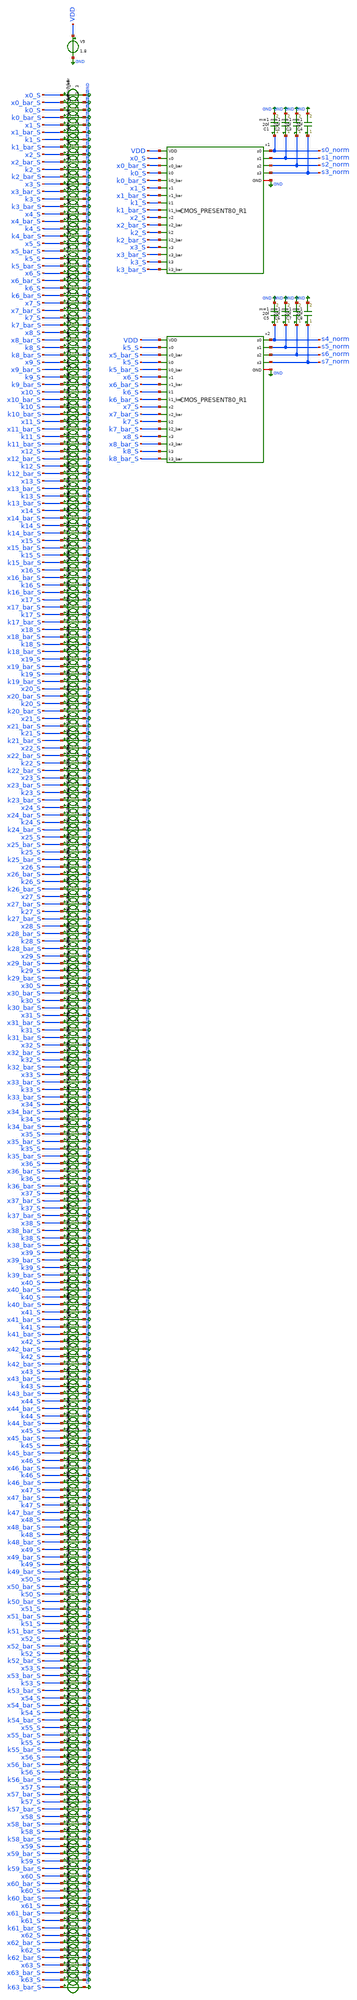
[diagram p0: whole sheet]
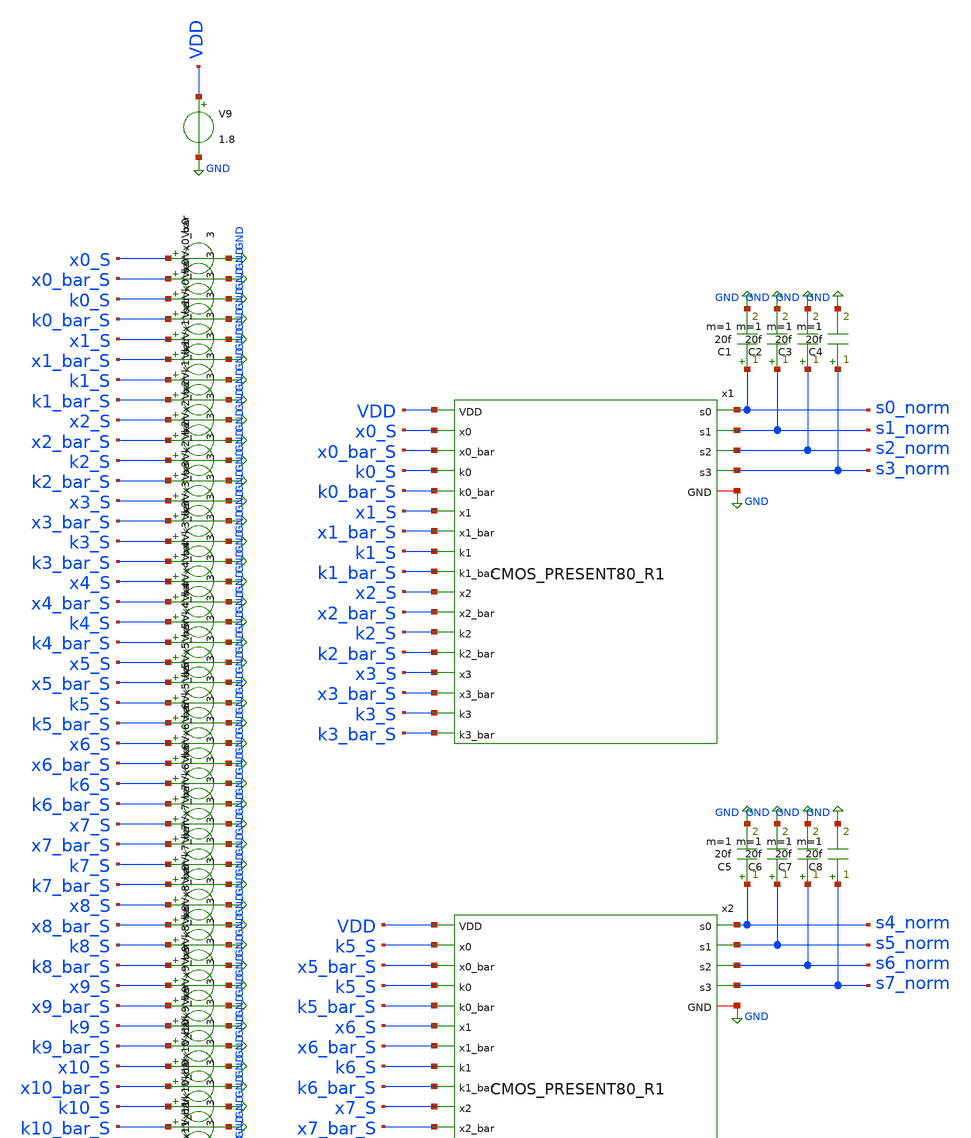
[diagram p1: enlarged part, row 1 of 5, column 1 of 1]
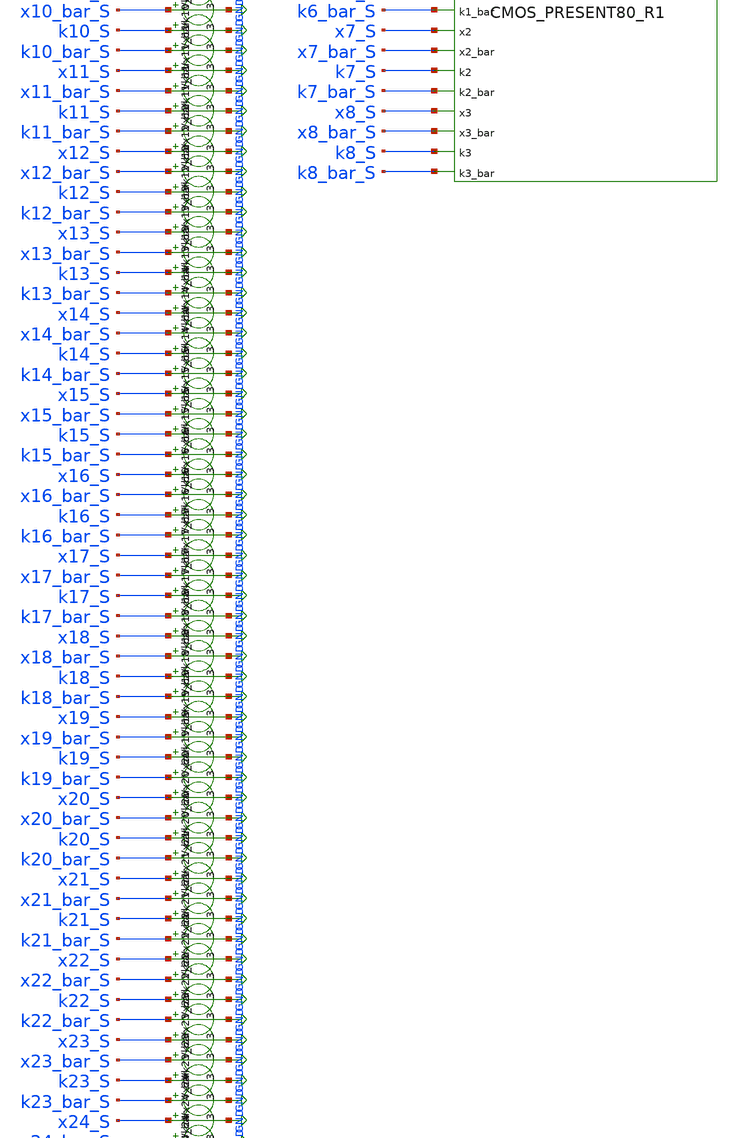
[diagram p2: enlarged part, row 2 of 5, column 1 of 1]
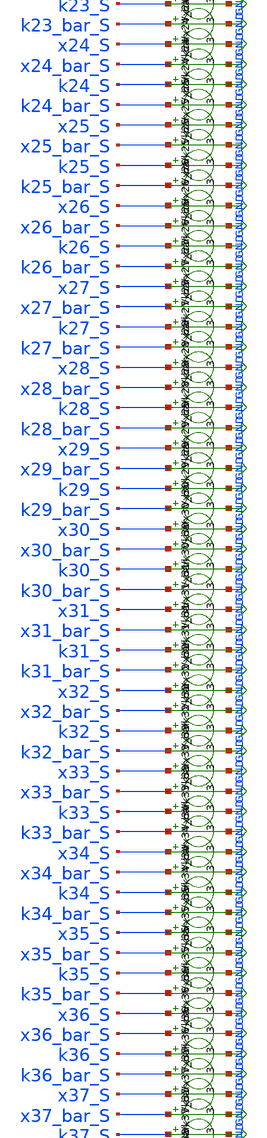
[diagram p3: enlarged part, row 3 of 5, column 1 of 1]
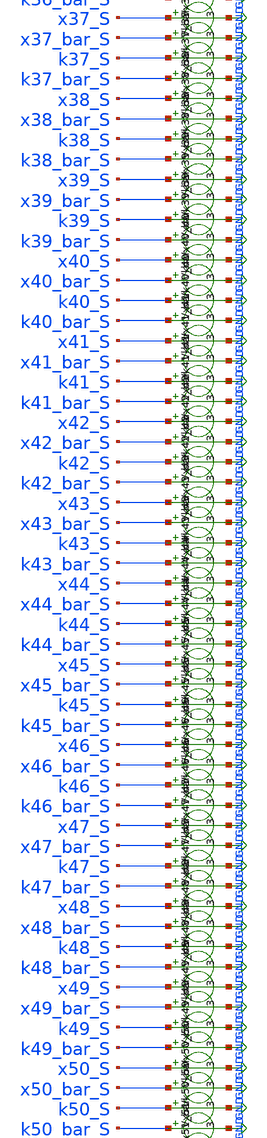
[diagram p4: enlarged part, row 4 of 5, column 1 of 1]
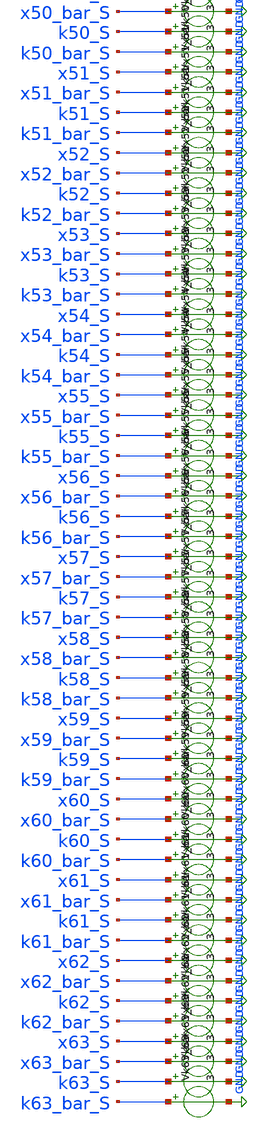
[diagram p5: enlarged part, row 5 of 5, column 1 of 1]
** sch_path: skywater_stuff/CMOS_PRESENT80_R1_sim.sch
**.subckt CMOS_PRESENT80_R1_sim
V9 VDD GND 1.8
C1 s0_norm GND 20f m=1
C2 s1_norm GND 20f m=1
C3 s2_norm GND 20f m=1
C4 s3_norm GND 20f m=1
x1 VDD GND k0_S k0_bar_S x0_S x0_bar_S x1_bar_S x1_S k1_bar_S k1_S k2_S k2_bar_S x2_S x2_bar_S
+ x3_bar_S x3_S k3_bar_S k3_S s3_norm s2_norm s1_norm s0_norm CMOS_PRESENT80_R1
Vx0 x0_S GND 3
Vx0_bar x0_bar_S GND 3
Vk0 k0_S GND 3
Vk0_bar k0_bar_S GND 3
Vx1 x1_S GND 3
Vx1_bar x1_bar_S GND 3
Vk1 k1_S GND 3
Vk1_bar k1_bar_S GND 3
Vx2 x2_S GND 3
Vx2_bar x2_bar_S GND 3
Vk2 k2_S GND 3
Vk2_bar k2_bar_S GND 3
Vx3 x3_S GND 3
Vx3_bar x3_bar_S GND 3
Vk3 k3_S GND 3
Vk3_bar k3_bar_S GND 3
Vx4 x4_S GND 3
Vx4_bar x4_bar_S GND 3
Vk4 k4_S GND 3
Vk4_bar k4_bar_S GND 3
Vx5 x5_S GND 3
Vx5_bar x5_bar_S GND 3
Vk5 k5_S GND 3
Vk5_bar k5_bar_S GND 3
Vx6 x6_S GND 3
Vx6_bar x6_bar_S GND 3
Vk6 k6_S GND 3
Vk6_bar k6_bar_S GND 3
Vx7 x7_S GND 3
Vx7_bar x7_bar_S GND 3
Vk7 k7_S GND 3
Vk7_bar k7_bar_S GND 3
Vx8 x8_S GND 3
Vx8_bar x8_bar_S GND 3
Vk8 k8_S GND 3
Vk8_bar k8_bar_S GND 3
Vx9 x9_S GND 3
Vx9_bar x9_bar_S GND 3
Vk9 k9_S GND 3
Vk9_bar k9_bar_S GND 3
Vx10 x10_S GND 3
Vx10_bar x10_bar_S GND 3
Vk10 k10_S GND 3
Vk10_bar k10_bar_S GND 3
Vx11 x11_S GND 3
Vx11_bar x11_bar_S GND 3
Vk11 k11_S GND 3
Vk11_bar k11_bar_S GND 3
Vx12 x12_S GND 3
Vx12_bar x12_bar_S GND 3
Vk12 k12_S GND 3
Vk12_bar k12_bar_S GND 3
Vx13 x13_S GND 3
Vx13_bar x13_bar_S GND 3
Vk13 k13_S GND 3
Vk13_bar k13_bar_S GND 3
Vx14 x14_S GND 3
Vx14_bar x14_bar_S GND 3
Vk14 k14_S GND 3
Vk14_bar k14_bar_S GND 3
Vx15 x15_S GND 3
Vx15_bar x15_bar_S GND 3
Vk15 k15_S GND 3
Vk15_bar k15_bar_S GND 3
Vx16 x16_S GND 3
Vx16_bar x16_bar_S GND 3
Vk16 k16_S GND 3
Vk16_bar k16_bar_S GND 3
Vx17 x17_S GND 3
Vx17_bar x17_bar_S GND 3
Vk17 k17_S GND 3
Vk17_bar k17_bar_S GND 3
Vx18 x18_S GND 3
Vx18_bar x18_bar_S GND 3
Vk18 k18_S GND 3
Vk18_bar k18_bar_S GND 3
Vx19 x19_S GND 3
Vx19_bar x19_bar_S GND 3
Vk19 k19_S GND 3
Vk19_bar k19_bar_S GND 3
Vx20 x20_S GND 3
Vx20_bar x20_bar_S GND 3
Vk20 k20_S GND 3
Vk20_bar k20_bar_S GND 3
Vx21 x21_S GND 3
Vx21_bar x21_bar_S GND 3
Vk21 k21_S GND 3
Vk21_bar k21_bar_S GND 3
Vx22 x22_S GND 3
Vx22_bar x22_bar_S GND 3
Vk22 k22_S GND 3
Vk22_bar k22_bar_S GND 3
Vx23 x23_S GND 3
Vx23_bar x23_bar_S GND 3
Vk23 k23_S GND 3
Vk23_bar k23_bar_S GND 3
Vx24 x24_S GND 3
Vx24_bar x24_bar_S GND 3
Vk24 k24_S GND 3
Vk24_bar k24_bar_S GND 3
Vx25 x25_S GND 3
Vx25_bar x25_bar_S GND 3
Vk25 k25_S GND 3
Vk25_bar k25_bar_S GND 3
Vx26 x26_S GND 3
Vx26_bar x26_bar_S GND 3
Vk26 k26_S GND 3
Vk26_bar k26_bar_S GND 3
Vx27 x27_S GND 3
Vx27_bar x27_bar_S GND 3
Vk27 k27_S GND 3
Vk27_bar k27_bar_S GND 3
Vx28 x28_S GND 3
Vx28_bar x28_bar_S GND 3
Vk28 k28_S GND 3
Vk28_bar k28_bar_S GND 3
Vx29 x29_S GND 3
Vx29_bar x29_bar_S GND 3
Vk29 k29_S GND 3
Vk29_bar k29_bar_S GND 3
Vx30 x30_S GND 3
Vx30_bar x30_bar_S GND 3
Vk30 k30_S GND 3
Vk30_bar k30_bar_S GND 3
Vx31 x31_S GND 3
Vx31_bar x31_bar_S GND 3
Vk31 k31_S GND 3
Vk31_bar k31_bar_S GND 3
Vx32 x32_S GND 3
Vx32_bar x32_bar_S GND 3
Vk32 k32_S GND 3
Vk32_bar k32_bar_S GND 3
Vx33 x33_S GND 3
Vx33_bar x33_bar_S GND 3
Vk33 k33_S GND 3
Vk33_bar k33_bar_S GND 3
Vx34 x34_S GND 3
Vx34_bar x34_bar_S GND 3
Vk34 k34_S GND 3
Vk34_bar k34_bar_S GND 3
Vx35 x35_S GND 3
Vx35_bar x35_bar_S GND 3
Vk35 k35_S GND 3
Vk35_bar k35_bar_S GND 3
Vx36 x36_S GND 3
Vx36_bar x36_bar_S GND 3
Vk36 k36_S GND 3
Vk36_bar k36_bar_S GND 3
Vx37 x37_S GND 3
Vx37_bar x37_bar_S GND 3
Vk37 k37_S GND 3
Vk37_bar k37_bar_S GND 3
Vx38 x38_S GND 3
Vx38_bar x38_bar_S GND 3
Vk38 k38_S GND 3
Vk38_bar k38_bar_S GND 3
Vx39 x39_S GND 3
Vx39_bar x39_bar_S GND 3
Vk39 k39_S GND 3
Vk39_bar k39_bar_S GND 3
Vx40 x40_S GND 3
Vx40_bar x40_bar_S GND 3
Vk40 k40_S GND 3
Vk40_bar k40_bar_S GND 3
Vx41 x41_S GND 3
Vx41_bar x41_bar_S GND 3
Vk41 k41_S GND 3
Vk41_bar k41_bar_S GND 3
Vx42 x42_S GND 3
Vx42_bar x42_bar_S GND 3
Vk42 k42_S GND 3
Vk42_bar k42_bar_S GND 3
Vx43 x43_S GND 3
Vx43_bar x43_bar_S GND 3
Vk43 k43_S GND 3
Vk43_bar k43_bar_S GND 3
Vx44 x44_S GND 3
Vx44_bar x44_bar_S GND 3
Vk44 k44_S GND 3
Vk44_bar k44_bar_S GND 3
Vx45 x45_S GND 3
Vx45_bar x45_bar_S GND 3
Vk45 k45_S GND 3
Vk45_bar k45_bar_S GND 3
Vx46 x46_S GND 3
Vx46_bar x46_bar_S GND 3
Vk46 k46_S GND 3
Vk46_bar k46_bar_S GND 3
Vx47 x47_S GND 3
Vx47_bar x47_bar_S GND 3
Vk47 k47_S GND 3
Vk47_bar k47_bar_S GND 3
Vx48 x48_S GND 3
Vx48_bar x48_bar_S GND 3
Vk48 k48_S GND 3
Vk48_bar k48_bar_S GND 3
Vx49 x49_S GND 3
Vx49_bar x49_bar_S GND 3
Vk49 k49_S GND 3
Vk49_bar k49_bar_S GND 3
Vx50 x50_S GND 3
Vx50_bar x50_bar_S GND 3
Vk50 k50_S GND 3
Vk50_bar k50_bar_S GND 3
Vx51 x51_S GND 3
Vx51_bar x51_bar_S GND 3
Vk51 k51_S GND 3
Vk51_bar k51_bar_S GND 3
Vx52 x52_S GND 3
Vx52_bar x52_bar_S GND 3
Vk52 k52_S GND 3
Vk52_bar k52_bar_S GND 3
Vx53 x53_S GND 3
Vx53_bar x53_bar_S GND 3
Vk53 k53_S GND 3
Vk53_bar k53_bar_S GND 3
Vx54 x54_S GND 3
Vx54_bar x54_bar_S GND 3
Vk54 k54_S GND 3
Vk54_bar k54_bar_S GND 3
Vx55 x55_S GND 3
Vx55_bar x55_bar_S GND 3
Vk55 k55_S GND 3
Vk55_bar k55_bar_S GND 3
Vx56 x56_S GND 3
Vx56_bar x56_bar_S GND 3
Vk56 k56_S GND 3
Vk56_bar k56_bar_S GND 3
Vx57 x57_S GND 3
Vx57_bar x57_bar_S GND 3
Vk57 k57_S GND 3
Vk57_bar k57_bar_S GND 3
Vx58 x58_S GND 3
Vx58_bar x58_bar_S GND 3
Vk58 k58_S GND 3
Vk58_bar k58_bar_S GND 3
Vx59 x59_S GND 3
Vx59_bar x59_bar_S GND 3
Vk59 k59_S GND 3
Vk59_bar k59_bar_S GND 3
Vx60 x60_S GND 3
Vx60_bar x60_bar_S GND 3
Vk60 k60_S GND 3
Vk60_bar k60_bar_S GND 3
Vx61 x61_S GND 3
Vx61_bar x61_bar_S GND 3
Vk61 k61_S GND 3
Vk61_bar k61_bar_S GND 3
Vx62 x62_S GND 3
Vx62_bar x62_bar_S GND 3
Vk62 k62_S GND 3
Vk62_bar k62_bar_S GND 3
Vx63 x63_S GND 3
Vx63_bar x63_bar_S GND 3
Vk63 k63_S GND 3
Vk63_bar k63_bar_S GND 3
x2 VDD GND k5_S k5_bar_S k5_S x5_bar_S x6_bar_S x6_S k6_bar_S k6_S k7_S k7_bar_S x7_S x7_bar_S
+ x8_bar_S x8_S k8_bar_S k8_S s7_norm s6_norm s5_norm s4_norm CMOS_PRESENT80_R1
C5 s4_norm GND 20f m=1
C6 s5_norm GND 20f m=1
C7 s6_norm GND 20f m=1
C8 s7_norm GND 20f m=1
**** begin user architecture code

.lib /research/pdk/open_pdks/share/pdk/sky130A/libs.tech/ngspice/sky130.lib.spice tt
.include ~/magic_layout_stuff/CMOS_PRESENT80_R1.spice
**.include ~/magic_layout_stuff/CMOS_PRESENT80_R1_flat.spice
.param v0 ='0' v0_bar ='1.8' v1 ='0' v1_bar ='1.8' v2 ='0' v2_bar ='1.8' v3 ='0' v3_bar ='1.8'
.option method=gear
.control
set tstart=0
*set tstop=0
let index=0
let index2=1
let wstart = $tstart
let wstop = 0n
let key = 7
let total_time = 32
let cycle_index = 1
let bit_index = 0
	while bit_index < 8
		set bit = `./test.sh $&key $bit_index`
		alter Vk$bit_index = '$bit ? 1.8 : 0'
		alter Vk`echo $bit_index`_bar = '$bit ? 0 : 1.8'
		let bit_index = bit_index + 1
	end

	*set values_raw < circ_inputs_`echo $&cycle_index`.txt
	set values_raw < circ_inputs_not_rand_`echo $&cycle_index`.txt
	compose values values $values_raw
	echo stuff

	*let curr_time = index*80n

	while index2 < length(values)
		let wstop = $&index2*80n
		stop when time=$&wstop
		let index2 = $&index2+1
		echo $&index2
	end

	let tstop = length(values)*80n
	while index < length(values)
		let value = values[$&index]
		echo $&value
		echo going into altering
		let bit_index = bit_index + 1
		while bit_index < 8
			set bit = `./test.sh $&value $bit_index`
			alter Vx$bit_index = '$bit ? 1.8 : 0'
			alter Vx`echo $bit_index`_bar = '$bit ? 0 : 1.8'
			let bit_index = bit_index + 1
		end
		echo test stuff
		let index=index+1
		if index = 1
			tran 1n $&tstop 0 1n
		else
			resume
		end
	end

	let index = 0
	*let Pinst = v(VDD)*v9#branch
	*plot Pinst
	while index < length(values)

		let Pinst = v(VDD)*v9#branch
		*plot Pinst
		let lin-tstart = $&index*80ns
		let lin-tstop = $&lin-tstart + 80ns
		let lin-tstep = 0.1n
		linearize Pinst
		*plot v(pinst)
		*display
		set appendwrite
		*wrdata K`echo $&key`_`echo $&total_time`u_`echo $&cycle_index`cycle.csv Pinst
		*wrdata CMOS_K`echo $&key`_`echo $&total_time`u_`echo $&cycle_index`cycle_norm_notRand.csv Pinst
		*wrdata CMOS_K`echo $&key`_`echo $&total_time`u_`echo $&cycle_index`cycle_norm.csv Pinst
		*wrdata CMOS_K`echo $&key`_`echo $&total_time`u_`echo $&cycle_index`cycle_flat.csv Pinst
		wrdata CMOS_8bitwidth_K`echo $&key`_`echo $&total_time`u_`echo $&cycle_index`cycle.csv Pinst
		let index = index + 1
		*echo $plots
		setplot tran1
		destroy tran2
		*echo $plots
	end
	*plot v(pinst)

.endc


**** end user architecture code
**.ends
.GLOBAL GND
.end
